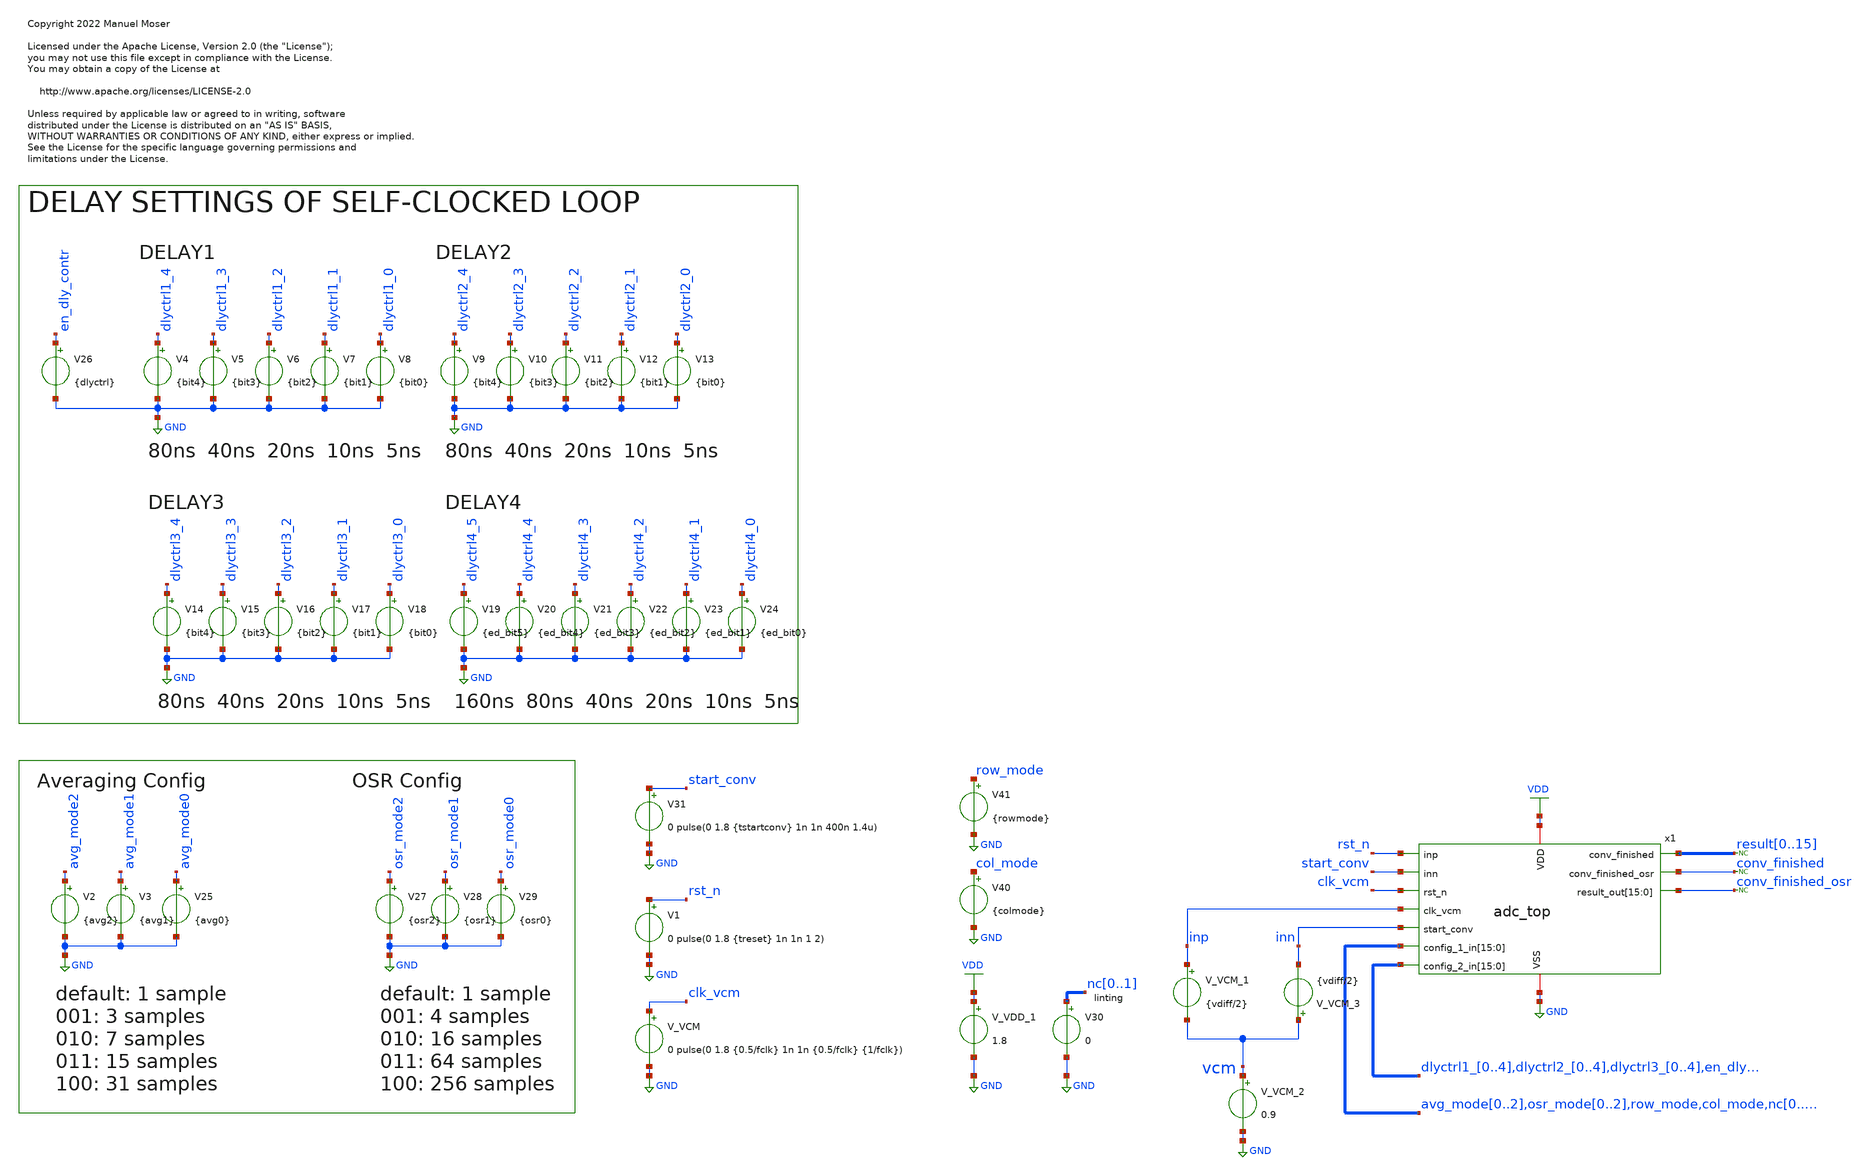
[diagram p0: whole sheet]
** sch_path: xschem/adc_top_tb.sch
* Copyright 2022 Manuel Moser
* Licensed under the Apache License, Version 2.0 (the "License");
**.subckt adc_top_tb
x1 VDD GND rst_n start_conv clk_vcm inp inn result0 conv_finished avg_mode0 avg_mode1 avg_mode2
+ osr_mode0 osr_mode1 osr_mode2 row_mode col_mode nc0 nc1 dlyctrl4_0 dlyctrl4_1 dlyctrl4_2 dlyctrl4_3
+ dlyctrl4_4 dlyctrl4_5 dlyctrl1_0 dlyctrl1_1 dlyctrl1_2 dlyctrl1_3 dlyctrl1_4 dlyctrl2_0 dlyctrl2_1 dlyctrl2_2
+ dlyctrl2_3 dlyctrl2_4 dlyctrl3_0 dlyctrl3_1 dlyctrl3_2 dlyctrl3_3 dlyctrl3_4 en_dly_contr conv_finished_osr
+ conv_finished_osr conv_finished_osr conv_finished_osr conv_finished_osr conv_finished_osr conv_finished_osr
+ conv_finished_osr conv_finished_osr conv_finished_osr conv_finished_osr conv_finished_osr conv_finished_osr
+ conv_finished_osr conv_finished_osr conv_finished_osr adc_top
V_VDD_1 VDD GND 1.8
V_VCM_2 vcm GND 0.9
* noconn result[0..15]
* noconn conv_finished
V_VCM_1 inp vcm {vdiff/2}
V_VCM_3 vcm inn {vdiff/2}
V_VCM clk_vcm GND 0 pulse(0 1.8 {0.5/fclk} 1n 1n {0.5/fclk} {1/fclk})
V1 rst_n GND 0 pulse(0 1.8 {treset} 1n 1n 1 2)
V31 start_conv GND 0 pulse(0 1.8 {tstartconv} 1n 1n 400n 1.4u)
V4 dlyctrl1_4 GND {bit4}
V5 dlyctrl1_3 GND {bit3}
V6 dlyctrl1_2 GND {bit2}
V7 dlyctrl1_1 GND {bit1}
V8 dlyctrl1_0 GND {bit0}
V2 avg_mode2 GND {avg2}
V3 avg_mode1 GND {avg1}
V25 avg_mode0 GND {avg0}
V19 dlyctrl4_5 GND {ed_bit5}
V20 dlyctrl4_4 GND {ed_bit4}
V21 dlyctrl4_3 GND {ed_bit3}
V22 dlyctrl4_2 GND {ed_bit2}
V23 dlyctrl4_1 GND {ed_bit1}
V24 dlyctrl4_0 GND {ed_bit0}
V26 en_dly_contr GND {dlyctrl}
V27 osr_mode2 GND {osr2}
V28 osr_mode1 GND {osr1}
V29 osr_mode0 GND {osr0}
V30 nc0 GND 0
V9 dlyctrl2_4 GND {bit4}
V10 dlyctrl2_3 GND {bit3}
V11 dlyctrl2_2 GND {bit2}
V12 dlyctrl2_1 GND {bit1}
V13 dlyctrl2_0 GND {bit0}
V14 dlyctrl3_4 GND {bit4}
V15 dlyctrl3_3 GND {bit3}
V16 dlyctrl3_2 GND {bit2}
V17 dlyctrl3_1 GND {bit1}
V18 dlyctrl3_0 GND {bit0}
* noconn conv_finished_osr
V40 col_mode GND {colmode}
V41 row_mode GND {rowmode}
**** begin user architecture code

** opencircuitdesign pdks install
.lib $::SKYWATER_MODELS/sky130.lib.spice tt





* ngspice commands
****************
* True mixed signal? (xspice) or analog? (spice)
****************
*.include /foss/designs/SKY130_SAR-ADC1/spice/adc_core_digital.spice
*.include /foss/designs/SKY130_SAR-ADC1/spice/adc_core_digital.v.xspice

.include adc_core_digital.v.xspice
.include adc_clkgen_with_edgedetect.gds.lvs.spice

*.include /foss/designs/SKY130_SAR-ADC1/spice/adc_clkgen_with_edgedetect.gds.lvs.spice
*.include /foss/designs/SKY130_SAR-ADC1/xspice/adc_clkgen_with_edgedetect.xspice

* mind the order: include AFTER XSPICE FILES
*.include /foss/pdks/sky130A/libs.ref/sky130_fd_sc_hd/spice/sky130_fd_sc_hd.spice


****************
* Misc
****************
.param fclk=32768
.param treset=100n
.param tstartconv=500n
.param vdiff=200m

****************
* Delay Config
****************
.param dlyctrl = 1.8

* delay 1-3
.param bit0 = 0
.param bit1 = 1.8
.param bit2 = 0
.param bit3 = 0
.param bit4 = 0

* edgedetect pulse
.param ed_bit0 = 0
.param ed_bit1 = 0
.param ed_bit2 = 1.8
.param ed_bit3 = 1.8
.param ed_bit4 = 0
.param ed_bit5 = 0

****************
* Averaging Config
****************
.param avg0 = 0
.param avg1 = 0
.param avg2 = 0

****************
* OSR Config
****************
.param osr0 = 0
.param osr1 = 0
.param osr2 = 0

***************
* ROW COL mode
***************
.param rowmode = 1.8
.param colmode = 1.8


.save all
.control
set num_threads=12
tran 250p 1.6u

plot inp inn rst_n start_conv conv_finished
plot start_conv x1.clk_dig x1.clk_comp
plot x1.pctop x1.nctop x1.comparator_result
plot x1.pctop-x1.nctop

let k = length(time) - 1

* Print the result vector at the end of tran
print result15[k] result14[k] result13[k] result12[k] result11[k] result10[k] result9[k] result8[k]
+ result7[k] result6[k] result5[k] result4[k] result3[k] result2[k] result1[k] result0[k]
* Print the result diff-voltage at the end of tran
print
+ (((result15[k]*2048+result14[k]*1024+result13[k]*512+result12[k]*256+result11[k]*128+result10[k]*64+result9[k]*32+result8[k]*16+result7[k]*8+result6[k]*4+result5[k]*2+result4[k]*1+result3[k]*0.5+result2[k]*0.25+result1[k]*0.125+result0[k]*0.0625)-2048*1.8)/2048)

set wr_vecnames
write adc_top_tb.raw inp inn rst_n start_conv conv_finished conv_finished_osr start_conv x1.clk_dig
+ x1.clk_comp x1.pctop x1.nctop x1.comparator_result result0 result1 result2 result3 result4 result5 result6
+ result7 result8 result9 result10 result11 result12 result13 result14 result15
.endc






**** end user architecture code
**.ends
.GLOBAL VDD
.GLOBAL GND
.end
